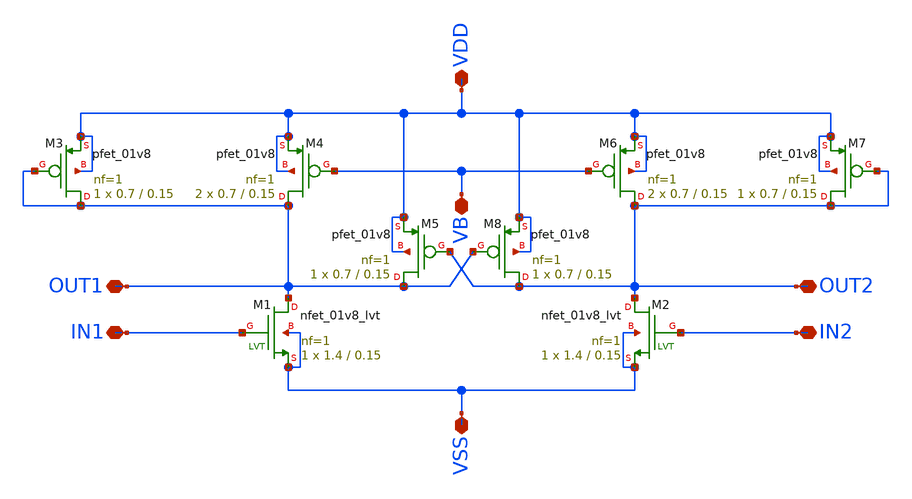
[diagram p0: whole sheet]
** sch_path: delay_cell_2.sch
**.subckt delay_cell_2 VDD VSS VB IN1 IN2 OUT2 OUT1
*.iopin VDD
*.iopin VSS
*.iopin VB
*.iopin IN1
*.iopin IN2
*.iopin OUT2
*.iopin OUT1
XM5 OUT1 OUT2 VDD VDD sky130_fd_pr__pfet_01v8 L=0.15 W=0.7 nf=1 ad='int((nf+1)/2) * W/nf * 0.29' as='int((nf+2)/2) * W/nf * 0.29'
+ pd='2*int((nf+1)/2) * (W/nf + 0.29)' ps='2*int((nf+2)/2) * (W/nf + 0.29)' nrd='0.29 / W' nrs='0.29 / W'
+ sa=0 sb=0 sd=0 mult=1 m=1
XM8 OUT2 OUT1 VDD VDD sky130_fd_pr__pfet_01v8 L=0.15 W=0.7 nf=1 ad='int((nf+1)/2) * W/nf * 0.29' as='int((nf+2)/2) * W/nf * 0.29'
+ pd='2*int((nf+1)/2) * (W/nf + 0.29)' ps='2*int((nf+2)/2) * (W/nf + 0.29)' nrd='0.29 / W' nrs='0.29 / W'
+ sa=0 sb=0 sd=0 mult=1 m=1
XM3 OUT1 OUT1 VDD VDD sky130_fd_pr__pfet_01v8 L=0.15 W=0.7 nf=1 ad='int((nf+1)/2) * W/nf * 0.29' as='int((nf+2)/2) * W/nf * 0.29'
+ pd='2*int((nf+1)/2) * (W/nf + 0.29)' ps='2*int((nf+2)/2) * (W/nf + 0.29)' nrd='0.29 / W' nrs='0.29 / W'
+ sa=0 sb=0 sd=0 mult=1 m=1
XM4 OUT1 VB VDD VDD sky130_fd_pr__pfet_01v8 L=0.15 W=0.7 nf=1 ad='int((nf+1)/2) * W/nf * 0.29' as='int((nf+2)/2) * W/nf * 0.29'
+ pd='2*int((nf+1)/2) * (W/nf + 0.29)' ps='2*int((nf+2)/2) * (W/nf + 0.29)' nrd='0.29 / W' nrs='0.29 / W'
+ sa=0 sb=0 sd=0 mult=2 m=2
XM6 OUT2 VB VDD VDD sky130_fd_pr__pfet_01v8 L=0.15 W=0.7 nf=1 ad='int((nf+1)/2) * W/nf * 0.29' as='int((nf+2)/2) * W/nf * 0.29'
+ pd='2*int((nf+1)/2) * (W/nf + 0.29)' ps='2*int((nf+2)/2) * (W/nf + 0.29)' nrd='0.29 / W' nrs='0.29 / W'
+ sa=0 sb=0 sd=0 mult=2 m=2
XM7 OUT2 OUT2 VDD VDD sky130_fd_pr__pfet_01v8 L=0.15 W=0.7 nf=1 ad='int((nf+1)/2) * W/nf * 0.29' as='int((nf+2)/2) * W/nf * 0.29'
+ pd='2*int((nf+1)/2) * (W/nf + 0.29)' ps='2*int((nf+2)/2) * (W/nf + 0.29)' nrd='0.29 / W' nrs='0.29 / W'
+ sa=0 sb=0 sd=0 mult=1 m=1
XM1 OUT1 IN1 VSS VSS sky130_fd_pr__nfet_01v8_lvt L=0.15 W=1.4 nf=1 ad='int((nf+1)/2) * W/nf * 0.29' as='int((nf+2)/2) * W/nf * 0.29'
+ pd='2*int((nf+1)/2) * (W/nf + 0.29)' ps='2*int((nf+2)/2) * (W/nf + 0.29)' nrd='0.29 / W' nrs='0.29 / W'
+ sa=0 sb=0 sd=0 mult=1 m=1
XM2 OUT2 IN2 VSS VSS sky130_fd_pr__nfet_01v8_lvt L=0.15 W=1.4 nf=1 ad='int((nf+1)/2) * W/nf * 0.29' as='int((nf+2)/2) * W/nf * 0.29'
+ pd='2*int((nf+1)/2) * (W/nf + 0.29)' ps='2*int((nf+2)/2) * (W/nf + 0.29)' nrd='0.29 / W' nrs='0.29 / W'
+ sa=0 sb=0 sd=0 mult=1 m=1
**.ends
.end
